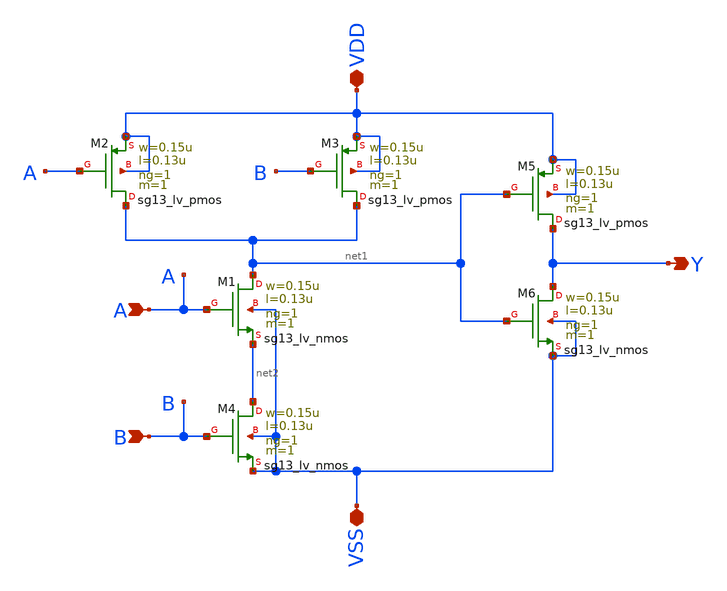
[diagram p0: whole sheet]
** sch_path: logic_gate/AND2/LAYOUT_POST-SIMULATION/AND2.sch
**.subckt AND2 A B Y VDD VSS
*.ipin A
*.ipin B
*.opin Y
*.iopin VDD
*.iopin VSS
XM1 net1 A net2 VSS sg13_lv_nmos w=0.15u l=0.13u ng=1 m=1 mm_ok=1
XM2 net1 A VDD VDD sg13_lv_pmos w=0.15u l=0.13u ng=1 m=1 mm_ok=1
XM3 net1 B VDD VDD sg13_lv_pmos w=0.15u l=0.13u ng=1 m=1 mm_ok=1
XM4 net2 B VSS VSS sg13_lv_nmos w=0.15u l=0.13u ng=1 m=1 mm_ok=1
XM5 Y net1 VDD VDD sg13_lv_pmos w=0.15u l=0.13u ng=1 m=1 mm_ok=1
XM6 Y net1 VSS VSS sg13_lv_nmos w=0.15u l=0.13u ng=1 m=1 mm_ok=1
**.ends
.end
